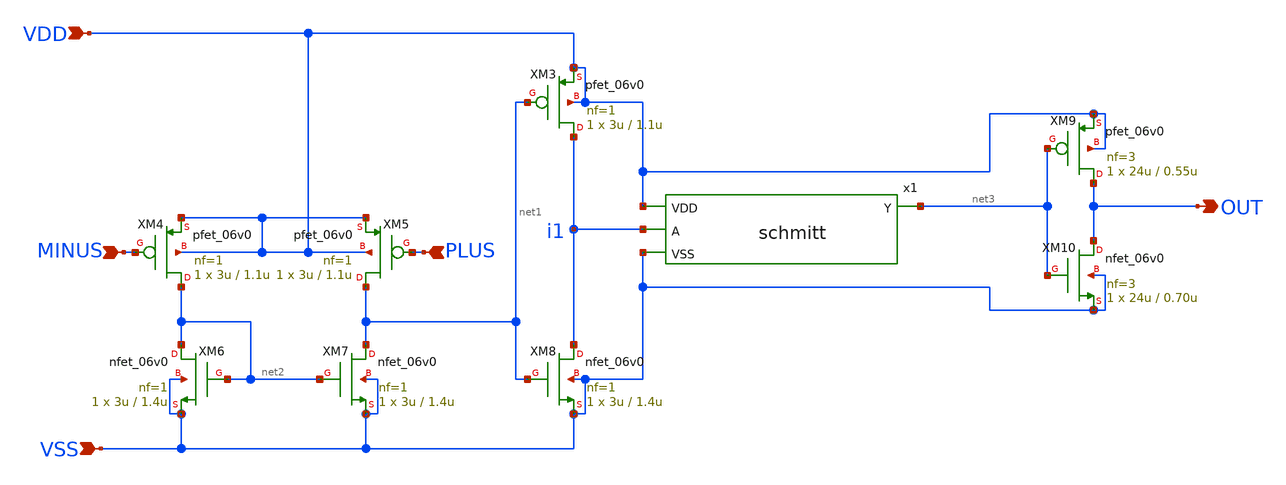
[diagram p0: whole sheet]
** sch_path: analog/xschem/comparator.sch
**.subckt comparator VDD PLUS VSS OUT MINUS
*.ipin VDD
*.ipin PLUS
*.ipin VSS
*.opin OUT
*.ipin MINUS
XM3 i1 net1 VDD VDD pfet_06v0 L=1.1u W=3u nf=1 ad='int((nf+1)/2) * W/nf * 0.18u' as='int((nf+2)/2) * W/nf * 0.18u'
+ pd='2*int((nf+1)/2) * (W/nf + 0.18u)' ps='2*int((nf+2)/2) * (W/nf + 0.18u)' nrd='0.18u / W' nrs='0.18u / W'
+ sa=0 sb=0 sd=0 m=1
XM4 net2 MINUS VDD VDD pfet_06v0 L=1.1u W=3u nf=1 ad='int((nf+1)/2) * W/nf * 0.18u' as='int((nf+2)/2) * W/nf * 0.18u'
+ pd='2*int((nf+1)/2) * (W/nf + 0.18u)' ps='2*int((nf+2)/2) * (W/nf + 0.18u)' nrd='0.18u / W' nrs='0.18u / W'
+ sa=0 sb=0 sd=0 m=1
XM5 net1 PLUS VDD VDD pfet_06v0 L=1.1u W=3u nf=1 ad='int((nf+1)/2) * W/nf * 0.18u' as='int((nf+2)/2) * W/nf * 0.18u'
+ pd='2*int((nf+1)/2) * (W/nf + 0.18u)' ps='2*int((nf+2)/2) * (W/nf + 0.18u)' nrd='0.18u / W' nrs='0.18u / W'
+ sa=0 sb=0 sd=0 m=1
XM6 net2 net2 VSS VSS nfet_06v0 L=1.4u W=3u nf=1 ad='int((nf+1)/2) * W/nf * 0.18u' as='int((nf+2)/2) * W/nf * 0.18u'
+ pd='2*int((nf+1)/2) * (W/nf + 0.18u)' ps='2*int((nf+2)/2) * (W/nf + 0.18u)' nrd='0.18u / W' nrs='0.18u / W'
+ sa=0 sb=0 sd=0 m=1
XM7 net1 net2 VSS VSS nfet_06v0 L=1.4u W=3u nf=1 ad='int((nf+1)/2) * W/nf * 0.18u' as='int((nf+2)/2) * W/nf * 0.18u'
+ pd='2*int((nf+1)/2) * (W/nf + 0.18u)' ps='2*int((nf+2)/2) * (W/nf + 0.18u)' nrd='0.18u / W' nrs='0.18u / W'
+ sa=0 sb=0 sd=0 m=1
XM8 i1 net1 VSS VSS nfet_06v0 L=1.4u W=3u nf=1 ad='int((nf+1)/2) * W/nf * 0.18u' as='int((nf+2)/2) * W/nf * 0.18u'
+ pd='2*int((nf+1)/2) * (W/nf + 0.18u)' ps='2*int((nf+2)/2) * (W/nf + 0.18u)' nrd='0.18u / W' nrs='0.18u / W'
+ sa=0 sb=0 sd=0 m=1
x1 VDD i1 net3 VSS schmitt
XM9 OUT net3 VDD VDD pfet_06v0 L=0.55u W=24u nf=3 ad='int((nf+1)/2) * W/nf * 0.18u' as='int((nf+2)/2) * W/nf * 0.18u'
+ pd='2*int((nf+1)/2) * (W/nf + 0.18u)' ps='2*int((nf+2)/2) * (W/nf + 0.18u)' nrd='0.18u / W' nrs='0.18u / W'
+ sa=0 sb=0 sd=0 m=1
XM10 OUT net3 VSS VSS nfet_06v0 L=0.70u W=24u nf=3 ad='int((nf+1)/2) * W/nf * 0.18u' as='int((nf+2)/2) * W/nf * 0.18u'
+ pd='2*int((nf+1)/2) * (W/nf + 0.18u)' ps='2*int((nf+2)/2) * (W/nf + 0.18u)' nrd='0.18u / W' nrs='0.18u / W'
+ sa=0 sb=0 sd=0 m=1
**.ends

* expanding   symbol:  schmitt.sym # of pins=4
** sym_path: analog/xschem/schmitt.sym
** sch_path: analog/xschem/schmitt.sch
.subckt schmitt VDD A Y VSS
*.ipin VDD
*.ipin VSS
*.ipin A
*.opin Y
XM1 net1 A VDD VDD pfet_06v0 L=0.55u W=4u nf=1 ad='int((nf+1)/2) * W/nf * 0.18u' as='int((nf+2)/2) * W/nf * 0.18u'
+ pd='2*int((nf+1)/2) * (W/nf + 0.18u)' ps='2*int((nf+2)/2) * (W/nf + 0.18u)' nrd='0.18u / W' nrs='0.18u / W'
+ sa=0 sb=0 sd=0 m=1
XM2 Y A net1 VDD pfet_06v0 L=0.55u W=4u nf=1 ad='int((nf+1)/2) * W/nf * 0.18u' as='int((nf+2)/2) * W/nf * 0.18u'
+ pd='2*int((nf+1)/2) * (W/nf + 0.18u)' ps='2*int((nf+2)/2) * (W/nf + 0.18u)' nrd='0.18u / W' nrs='0.18u / W'
+ sa=0 sb=0 sd=0 m=1
XM3 Y A net2 VSS nfet_06v0 L=0.70u W=4u nf=1 ad='int((nf+1)/2) * W/nf * 0.18u' as='int((nf+2)/2) * W/nf * 0.18u'
+ pd='2*int((nf+1)/2) * (W/nf + 0.18u)' ps='2*int((nf+2)/2) * (W/nf + 0.18u)' nrd='0.18u / W' nrs='0.18u / W'
+ sa=0 sb=0 sd=0 m=1
XM4 net2 A VSS VSS nfet_06v0 L=0.70u W=4u nf=1 ad='int((nf+1)/2) * W/nf * 0.18u' as='int((nf+2)/2) * W/nf * 0.18u'
+ pd='2*int((nf+1)/2) * (W/nf + 0.18u)' ps='2*int((nf+2)/2) * (W/nf + 0.18u)' nrd='0.18u / W' nrs='0.18u / W'
+ sa=0 sb=0 sd=0 m=1
XM5 VSS Y net1 VDD pfet_06v0 L=0.55u W=2u nf=1 ad='int((nf+1)/2) * W/nf * 0.18u' as='int((nf+2)/2) * W/nf * 0.18u'
+ pd='2*int((nf+1)/2) * (W/nf + 0.18u)' ps='2*int((nf+2)/2) * (W/nf + 0.18u)' nrd='0.18u / W' nrs='0.18u / W'
+ sa=0 sb=0 sd=0 m=1
XM6 VDD Y net2 VSS nfet_06v0 L=0.70u W=2u nf=1 ad='int((nf+1)/2) * W/nf * 0.18u' as='int((nf+2)/2) * W/nf * 0.18u'
+ pd='2*int((nf+1)/2) * (W/nf + 0.18u)' ps='2*int((nf+2)/2) * (W/nf + 0.18u)' nrd='0.18u / W' nrs='0.18u / W'
+ sa=0 sb=0 sd=0 m=1
.ends

.end
